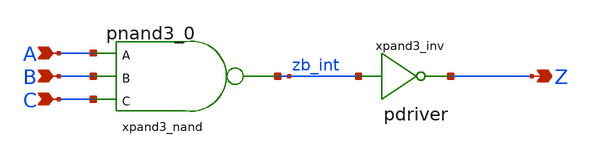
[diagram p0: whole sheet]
** sch_path: sram_4_16_scn4m/pand3.sch
**.subckt pand3 A B C Z
*.ipin A
*.ipin B
*.ipin C
*.opin Z
xpand3_nand A B C zb_int vdd gnd pnand3_0
xpand3_inv zb_int Z vdd gnd pdriver
**.ends

* expanding   symbol:  pnand3_0.sym # of pins=4
** sym_path: sram_4_16_scn4m/pnand3_0.sym
** sch_path: sram_4_16_scn4m/pnand3_0.sch
.subckt pnand3_0 A B C Z vdd gnd
*.ipin C
*.ipin A
*.ipin B
*.opin Z
*.iopin vdd
*.iopin gnd
XMpnand3_nmos1 Z C net1 gnd sky130_fd_pr__nfet_01v8 L=0.4 W=1.6 nf=1 ad='int((nf+1)/2) * W/nf * 0.29'
+ as='int((nf+2)/2) * W/nf * 0.29' pd='2*int((nf+1)/2) * (W/nf + 0.29)' ps='2*int((nf+2)/2) * (W/nf + 0.29)'
+ nrd='0.29 / W' nrs='0.29 / W' sa=0 sb=0 sd=0 mult=1 m=1
XMpnand3_pmos1 Z A vdd vdd sky130_fd_pr__pfet_01v8 L=0.4 W=1.6 nf=1 ad='int((nf+1)/2) * W/nf * 0.29'
+ as='int((nf+2)/2) * W/nf * 0.29' pd='2*int((nf+1)/2) * (W/nf + 0.29)' ps='2*int((nf+2)/2) * (W/nf + 0.29)'
+ nrd='0.29 / W' nrs='0.29 / W' sa=0 sb=0 sd=0 mult=1 m=1
XMpnand3_pmos3 Z C vdd vdd sky130_fd_pr__pfet_01v8 L=0.4 W=1.6 nf=1 ad='int((nf+1)/2) * W/nf * 0.29'
+ as='int((nf+2)/2) * W/nf * 0.29' pd='2*int((nf+1)/2) * (W/nf + 0.29)' ps='2*int((nf+2)/2) * (W/nf + 0.29)'
+ nrd='0.29 / W' nrs='0.29 / W' sa=0 sb=0 sd=0 mult=1 m=1
XMpnand3_nmos2 net1 B net2 gnd sky130_fd_pr__nfet_01v8 L=0.4 W=1.6 nf=1 ad='int((nf+1)/2) * W/nf * 0.29'
+ as='int((nf+2)/2) * W/nf * 0.29' pd='2*int((nf+1)/2) * (W/nf + 0.29)' ps='2*int((nf+2)/2) * (W/nf + 0.29)'
+ nrd='0.29 / W' nrs='0.29 / W' sa=0 sb=0 sd=0 mult=1 m=1
XMpnand3_pmos2 Z B vdd vdd sky130_fd_pr__pfet_01v8 L=0.4 W=1.6 nf=1 ad='int((nf+1)/2) * W/nf * 0.29'
+ as='int((nf+2)/2) * W/nf * 0.29' pd='2*int((nf+1)/2) * (W/nf + 0.29)' ps='2*int((nf+2)/2) * (W/nf + 0.29)'
+ nrd='0.29 / W' nrs='0.29 / W' sa=0 sb=0 sd=0 mult=1 m=1
XMpnand3_nmos3 net2 A gnd gnd sky130_fd_pr__nfet_01v8 L=0.4 W=1.6 nf=1 ad='int((nf+1)/2) * W/nf * 0.29'
+ as='int((nf+2)/2) * W/nf * 0.29' pd='2*int((nf+1)/2) * (W/nf + 0.29)' ps='2*int((nf+2)/2) * (W/nf + 0.29)'
+ nrd='0.29 / W' nrs='0.29 / W' sa=0 sb=0 sd=0 mult=1 m=1
.ends


* expanding   symbol:  pdriver.sym # of pins=2
** sym_path: sram_4_16_scn4m/pdriver.sym
** sch_path: sram_4_16_scn4m/pdriver.sch
.subckt pdriver A Z vdd gnd
*.ipin A
*.opin Z
xbuf_inv1 A Z vdd gnd pinv_2
.ends


* expanding   symbol:  pinv_2.sym # of pins=2
** sym_path: sram_2_64_scn4m/pinv_2.sym
** sch_path: sram_2_64_scn4m/pinv_2.sch
.subckt pinv_2 A Z vdd gnd
*.ipin A
*.opin Z
Mpinv_nmos Z A gnd gnd n w=0.8u l=0.4u m=1
Mp_inv_pmos Z A vdd vdd p w=1.6u l=0.4u m=1
.ends

.end
